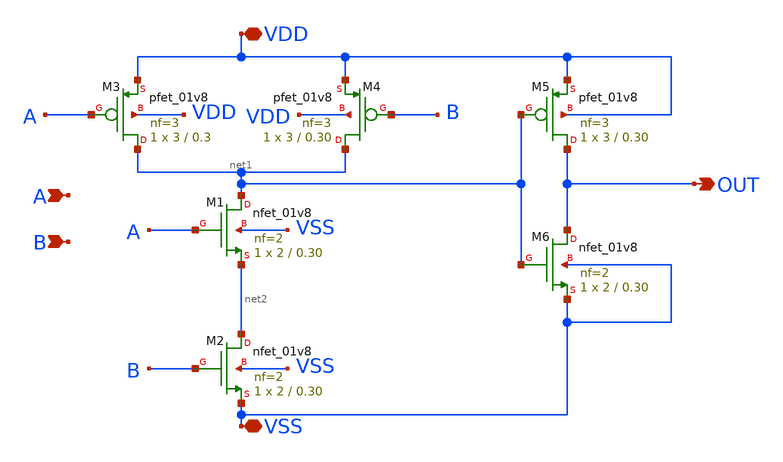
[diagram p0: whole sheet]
** sch_path: design/CONTROL_UNIT/xschem/and2.sch
**.subckt and2 VSS A B VDD OUT
*.iopin VSS
*.ipin A
*.ipin B
*.iopin VDD
*.opin OUT
XM2 net2 B VSS VSS sky130_fd_pr__nfet_01v8 L=0.30 W=2 nf=2 ad='int((nf+1)/2) * W/nf * 0.29' as='int((nf+2)/2) * W/nf * 0.29'
+ pd='2*int((nf+1)/2) * (W/nf + 0.29)' ps='2*int((nf+2)/2) * (W/nf + 0.29)' nrd='0.29 / W' nrs='0.29 / W'
+ sa=0 sb=0 sd=0 mult=1 m=1
XM1 net1 A net2 VSS sky130_fd_pr__nfet_01v8 L=0.30 W=2 nf=2 ad='int((nf+1)/2) * W/nf * 0.29' as='int((nf+2)/2) * W/nf * 0.29'
+ pd='2*int((nf+1)/2) * (W/nf + 0.29)' ps='2*int((nf+2)/2) * (W/nf + 0.29)' nrd='0.29 / W' nrs='0.29 / W'
+ sa=0 sb=0 sd=0 mult=1 m=1
XM3 net1 A VDD VDD sky130_fd_pr__pfet_01v8 L=0.3 W=3 nf=3 ad='int((nf+1)/2) * W/nf * 0.29' as='int((nf+2)/2) * W/nf * 0.29'
+ pd='2*int((nf+1)/2) * (W/nf + 0.29)' ps='2*int((nf+2)/2) * (W/nf + 0.29)' nrd='0.29 / W' nrs='0.29 / W'
+ sa=0 sb=0 sd=0 mult=1 m=1
XM4 net1 B VDD VDD sky130_fd_pr__pfet_01v8 L=0.30 W=3 nf=3 ad='int((nf+1)/2) * W/nf * 0.29' as='int((nf+2)/2) * W/nf * 0.29'
+ pd='2*int((nf+1)/2) * (W/nf + 0.29)' ps='2*int((nf+2)/2) * (W/nf + 0.29)' nrd='0.29 / W' nrs='0.29 / W'
+ sa=0 sb=0 sd=0 mult=1 m=1
XM5 OUT net1 VDD VDD sky130_fd_pr__pfet_01v8 L=0.30 W=3 nf=3 ad='int((nf+1)/2) * W/nf * 0.29' as='int((nf+2)/2) * W/nf * 0.29'
+ pd='2*int((nf+1)/2) * (W/nf + 0.29)' ps='2*int((nf+2)/2) * (W/nf + 0.29)' nrd='0.29 / W' nrs='0.29 / W'
+ sa=0 sb=0 sd=0 mult=1 m=1
XM6 OUT net1 VSS VSS sky130_fd_pr__nfet_01v8 L=0.30 W=2 nf=2 ad='int((nf+1)/2) * W/nf * 0.29' as='int((nf+2)/2) * W/nf * 0.29'
+ pd='2*int((nf+1)/2) * (W/nf + 0.29)' ps='2*int((nf+2)/2) * (W/nf + 0.29)' nrd='0.29 / W' nrs='0.29 / W'
+ sa=0 sb=0 sd=0 mult=1 m=1
**.ends
.end
